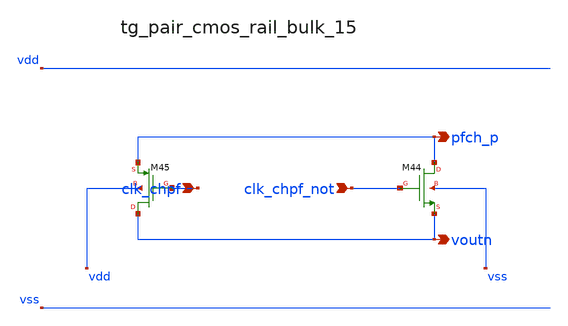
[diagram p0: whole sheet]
** sch_path: analog-db/raw/ia_003_fan_chopper_pf/hier/blocks/tg_pair_cmos_rail_bulk_15.sch
**.subckt tg_pair_cmos_rail_bulk_15 clk_chpf clk_chpf_not pfch_p voutn
*.ipin clk_chpf
*.ipin clk_chpf_not
*.opin pfch_p
*.opin voutn
XM44 pfch_p clk_chpf_not voutn vss sg13_lv_nmos w=x_dut_xm44_w l=x_dut_xm44_l ng=1 m=x_dut_xm44_m
XM45 voutn clk_chpf pfch_p vdd sg13_lv_pmos w=x_dut_xm45_w l=x_dut_xm45_l ng=1 m=x_dut_xm45_m
**.ends
.end
